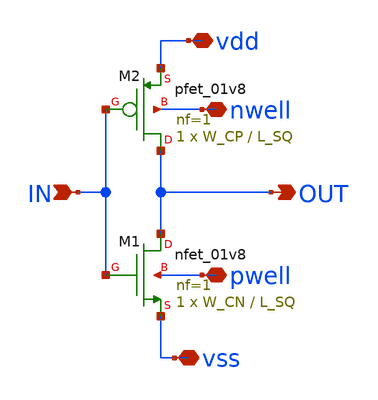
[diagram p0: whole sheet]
** sch_path: design/core/sqar_inv/sqar_inv.sch
**.subckt sqar_inv IN OUT nwell pwell vss vdd
*.ipin IN
*.opin OUT
*.iopin nwell
*.iopin pwell
*.iopin vss
*.iopin vdd
XM1 OUT IN vss pwell sky130_fd_pr__nfet_01v8 L=L_SQ W=W_CN nf=1 ad='int((nf+1)/2) * W/nf * 0.29' as='int((nf+2)/2) * W/nf * 0.29'
+ pd='2*int((nf+1)/2) * (W/nf + 0.29)' ps='2*int((nf+2)/2) * (W/nf + 0.29)' nrd='0.29 / W' nrs='0.29 / W'
+ sa=0 sb=0 sd=0 mult=1 m=1
XM2 OUT IN vdd nwell sky130_fd_pr__pfet_01v8 L=L_SQ W=W_CP nf=1 ad='int((nf+1)/2) * W/nf * 0.29' as='int((nf+2)/2) * W/nf * 0.29'
+ pd='2*int((nf+1)/2) * (W/nf + 0.29)' ps='2*int((nf+2)/2) * (W/nf + 0.29)' nrd='0.29 / W' nrs='0.29 / W'
+ sa=0 sb=0 sd=0 mult=1 m=1
**.ends
.end
